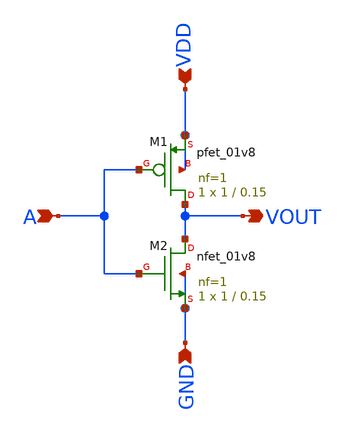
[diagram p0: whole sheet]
** sch_path: inverter/unv.sch
**.subckt unv A VDD GND VOUT
*.ipin A
*.ipin VDD
*.ipin GND
*.opin VOUT
XM1 VOUT A VDD VDD sky130_fd_pr__pfet_01v8 L=0.15 W=1 nf=1 ad='int((1 + 1)/2) * 1 / 1 * 0.29' as='int((1 + 2)/2) * 1 / 1 * 0.29'
+ pd='2*int((1 + 1)/2) * (1 / 1 + 0.29)' ps='2*int((1 + 2)/2) * (1 / 1 + 0.29)' nrd='0.29 / 1 ' nrs='0.29 / 1 '
+ sa=0 sb=0 sd=0 mult=1 m=1
XM2 VOUT A GND GND sky130_fd_pr__nfet_01v8 L=0.15 W=1 nf=1 ad='int((1 + 1)/2) * 1 / 1 * 0.29' as='int((1 + 2)/2) * 1 / 1 * 0.29'
+ pd='2*int((1 + 1)/2) * (1 / 1 + 0.29)' ps='2*int((1 + 2)/2) * (1 / 1 + 0.29)' nrd='0.29 / 1 ' nrs='0.29 / 1 '
+ sa=0 sb=0 sd=0 mult=1 m=1
**.ends
.end
